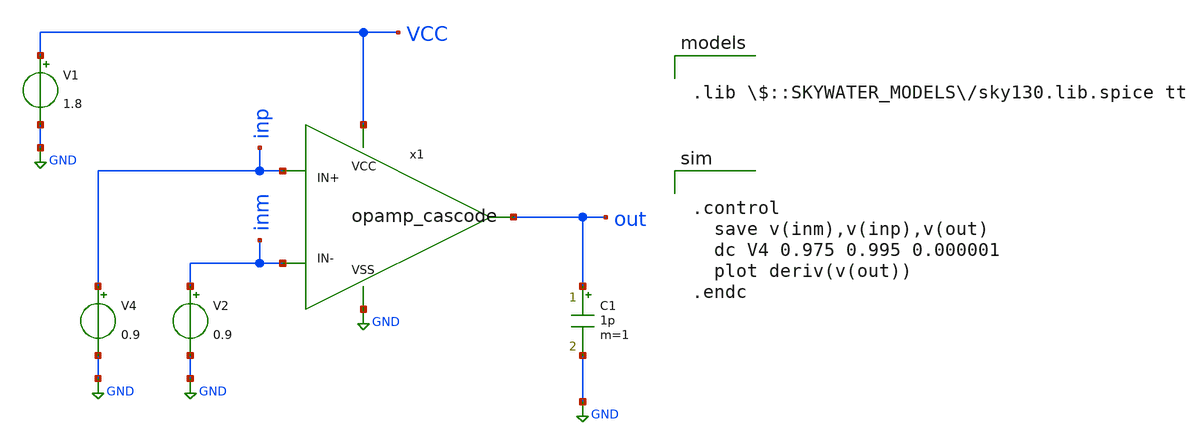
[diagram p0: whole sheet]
** sch_path: opamp_cascode_dc_response.sch
**.subckt opamp_cascode_dc_response
V1 VCC GND 1.8
V4 inp GND 0.9
V2 inm GND 0.9
C1 out GND 1p m=1
x1 VCC GND inp inm out opamp_cascode
**** begin user architecture code


.control
  save v(inm),v(inp),v(out)
  dc V4 0.975 0.995 0.000001
  plot deriv(v(out))
.endc



.lib $::SKYWATER_MODELS/sky130.lib.spice tt

**** end user architecture code
**.ends

* expanding   symbol:  /home/zwierzak/projects/SKY130_OpAmp_GIT/opamp_cascode.sym # of pins=5
** sym_path: opamp_cascode.sym
** sch_path: opamp_cascode.sch
.subckt opamp_cascode VCC VSS IN+ IN- OUT
*.ipin IN+
*.ipin IN-
*.ipin VCC
*.ipin VSS
*.opin OUT
XM10 net8 net6 VCC VCC sky130_fd_pr__pfet_01v8 L=10 W=40 nf=1 ad='int((nf+1)/2) * W/nf * 0.29' as='int((nf+2)/2) * W/nf * 0.29'
+ pd='2*int((nf+1)/2) * (W/nf + 0.29)' ps='2*int((nf+2)/2) * (W/nf + 0.29)' nrd='0.29 / W' nrs='0.29 / W'
+ sa=0 sb=0 sd=0 mult=2 m=2
XM1 net7 net6 VCC VCC sky130_fd_pr__pfet_01v8 L=10 W=40 nf=1 ad='int((nf+1)/2) * W/nf * 0.29' as='int((nf+2)/2) * W/nf * 0.29'
+ pd='2*int((nf+1)/2) * (W/nf + 0.29)' ps='2*int((nf+2)/2) * (W/nf + 0.29)' nrd='0.29 / W' nrs='0.29 / W'
+ sa=0 sb=0 sd=0 mult=2 m=2
XM5 net3 net9 VCC VCC sky130_fd_pr__pfet_01v8 L=3 W=20 nf=1 ad='int((nf+1)/2) * W/nf * 0.29' as='int((nf+2)/2) * W/nf * 0.29'
+ pd='2*int((nf+1)/2) * (W/nf + 0.29)' ps='2*int((nf+2)/2) * (W/nf + 0.29)' nrd='0.29 / W' nrs='0.29 / W'
+ sa=0 sb=0 sd=0 mult=10 m=10
XM100 net9 net9 VCC VCC sky130_fd_pr__pfet_01v8 L=3 W=20 nf=1 ad='int((nf+1)/2) * W/nf * 0.29' as='int((nf+2)/2) * W/nf * 0.29'
+ pd='2*int((nf+1)/2) * (W/nf + 0.29)' ps='2*int((nf+2)/2) * (W/nf + 0.29)' nrd='0.29 / W' nrs='0.29 / W'
+ sa=0 sb=0 sd=0 mult=1 m=1
I0 net9 VSS 3.5u
XM11 OUT BIAS net8 net8 sky130_fd_pr__pfet_01v8 L=3 W=20 nf=1 ad='int((nf+1)/2) * W/nf * 0.29' as='int((nf+2)/2) * W/nf * 0.29'
+ pd='2*int((nf+1)/2) * (W/nf + 0.29)' ps='2*int((nf+2)/2) * (W/nf + 0.29)' nrd='0.29 / W' nrs='0.29 / W'
+ sa=0 sb=0 sd=0 mult=10 m=10
XM2 net6 BIAS net7 net7 sky130_fd_pr__pfet_01v8 L=3 W=20 nf=1 ad='int((nf+1)/2) * W/nf * 0.29' as='int((nf+2)/2) * W/nf * 0.29'
+ pd='2*int((nf+1)/2) * (W/nf + 0.29)' ps='2*int((nf+2)/2) * (W/nf + 0.29)' nrd='0.29 / W' nrs='0.29 / W'
+ sa=0 sb=0 sd=0 mult=10 m=10
XM6 net1 IN- net3 net3 sky130_fd_pr__pfet_01v8 L=0.25 W=25 nf=2 ad='int((nf+1)/2) * W/nf * 0.29' as='int((nf+2)/2) * W/nf * 0.29'
+ pd='2*int((nf+1)/2) * (W/nf + 0.29)' ps='2*int((nf+2)/2) * (W/nf + 0.29)' nrd='0.29 / W' nrs='0.29 / W'
+ sa=0 sb=0 sd=0 mult=3 m=3
XM8 net2 IN+ net3 net3 sky130_fd_pr__pfet_01v8 L=0.25 W=25 nf=2 ad='int((nf+1)/2) * W/nf * 0.29' as='int((nf+2)/2) * W/nf * 0.29'
+ pd='2*int((nf+1)/2) * (W/nf + 0.29)' ps='2*int((nf+2)/2) * (W/nf + 0.29)' nrd='0.29 / W' nrs='0.29 / W'
+ sa=0 sb=0 sd=0 mult=3 m=3
XM7 net1 net1 VSS VSS sky130_fd_pr__nfet_01v8 L=10 W=20 nf=1 ad='int((nf+1)/2) * W/nf * 0.29' as='int((nf+2)/2) * W/nf * 0.29'
+ pd='2*int((nf+1)/2) * (W/nf + 0.29)' ps='2*int((nf+2)/2) * (W/nf + 0.29)' nrd='0.29 / W' nrs='0.29 / W'
+ sa=0 sb=0 sd=0 mult=1 m=1
XM9 net2 net2 VSS VSS sky130_fd_pr__nfet_01v8 L=10 W=20 nf=1 ad='int((nf+1)/2) * W/nf * 0.29' as='int((nf+2)/2) * W/nf * 0.29'
+ pd='2*int((nf+1)/2) * (W/nf + 0.29)' ps='2*int((nf+2)/2) * (W/nf + 0.29)' nrd='0.29 / W' nrs='0.29 / W'
+ sa=0 sb=0 sd=0 mult=1 m=1
XM13 net4 net2 VSS VSS sky130_fd_pr__nfet_01v8 L=10 W=20 nf=1 ad='int((nf+1)/2) * W/nf * 0.29' as='int((nf+2)/2) * W/nf * 0.29'
+ pd='2*int((nf+1)/2) * (W/nf + 0.29)' ps='2*int((nf+2)/2) * (W/nf + 0.29)' nrd='0.29 / W' nrs='0.29 / W'
+ sa=0 sb=0 sd=0 mult=3 m=3
XM4 net5 net1 VSS VSS sky130_fd_pr__nfet_01v8 L=10 W=20 nf=1 ad='int((nf+1)/2) * W/nf * 0.29' as='int((nf+2)/2) * W/nf * 0.29'
+ pd='2*int((nf+1)/2) * (W/nf + 0.29)' ps='2*int((nf+2)/2) * (W/nf + 0.29)' nrd='0.29 / W' nrs='0.29 / W'
+ sa=0 sb=0 sd=0 mult=3 m=3
XM12 OUT BIAS1 net4 net4 sky130_fd_pr__nfet_01v8 L=3 W=20 nf=1 ad='int((nf+1)/2) * W/nf * 0.29' as='int((nf+2)/2) * W/nf * 0.29'
+ pd='2*int((nf+1)/2) * (W/nf + 0.29)' ps='2*int((nf+2)/2) * (W/nf + 0.29)' nrd='0.29 / W' nrs='0.29 / W'
+ sa=0 sb=0 sd=0 mult=5 m=5
XM3 net6 BIAS1 net5 net5 sky130_fd_pr__nfet_01v8 L=3 W=20 nf=1 ad='int((nf+1)/2) * W/nf * 0.29' as='int((nf+2)/2) * W/nf * 0.29'
+ pd='2*int((nf+1)/2) * (W/nf + 0.29)' ps='2*int((nf+2)/2) * (W/nf + 0.29)' nrd='0.29 / W' nrs='0.29 / W'
+ sa=0 sb=0 sd=0 mult=5 m=5
V1 BIAS VSS 0
V2 BIAS1 VSS 0.6
.ends

.GLOBAL GND
.end
